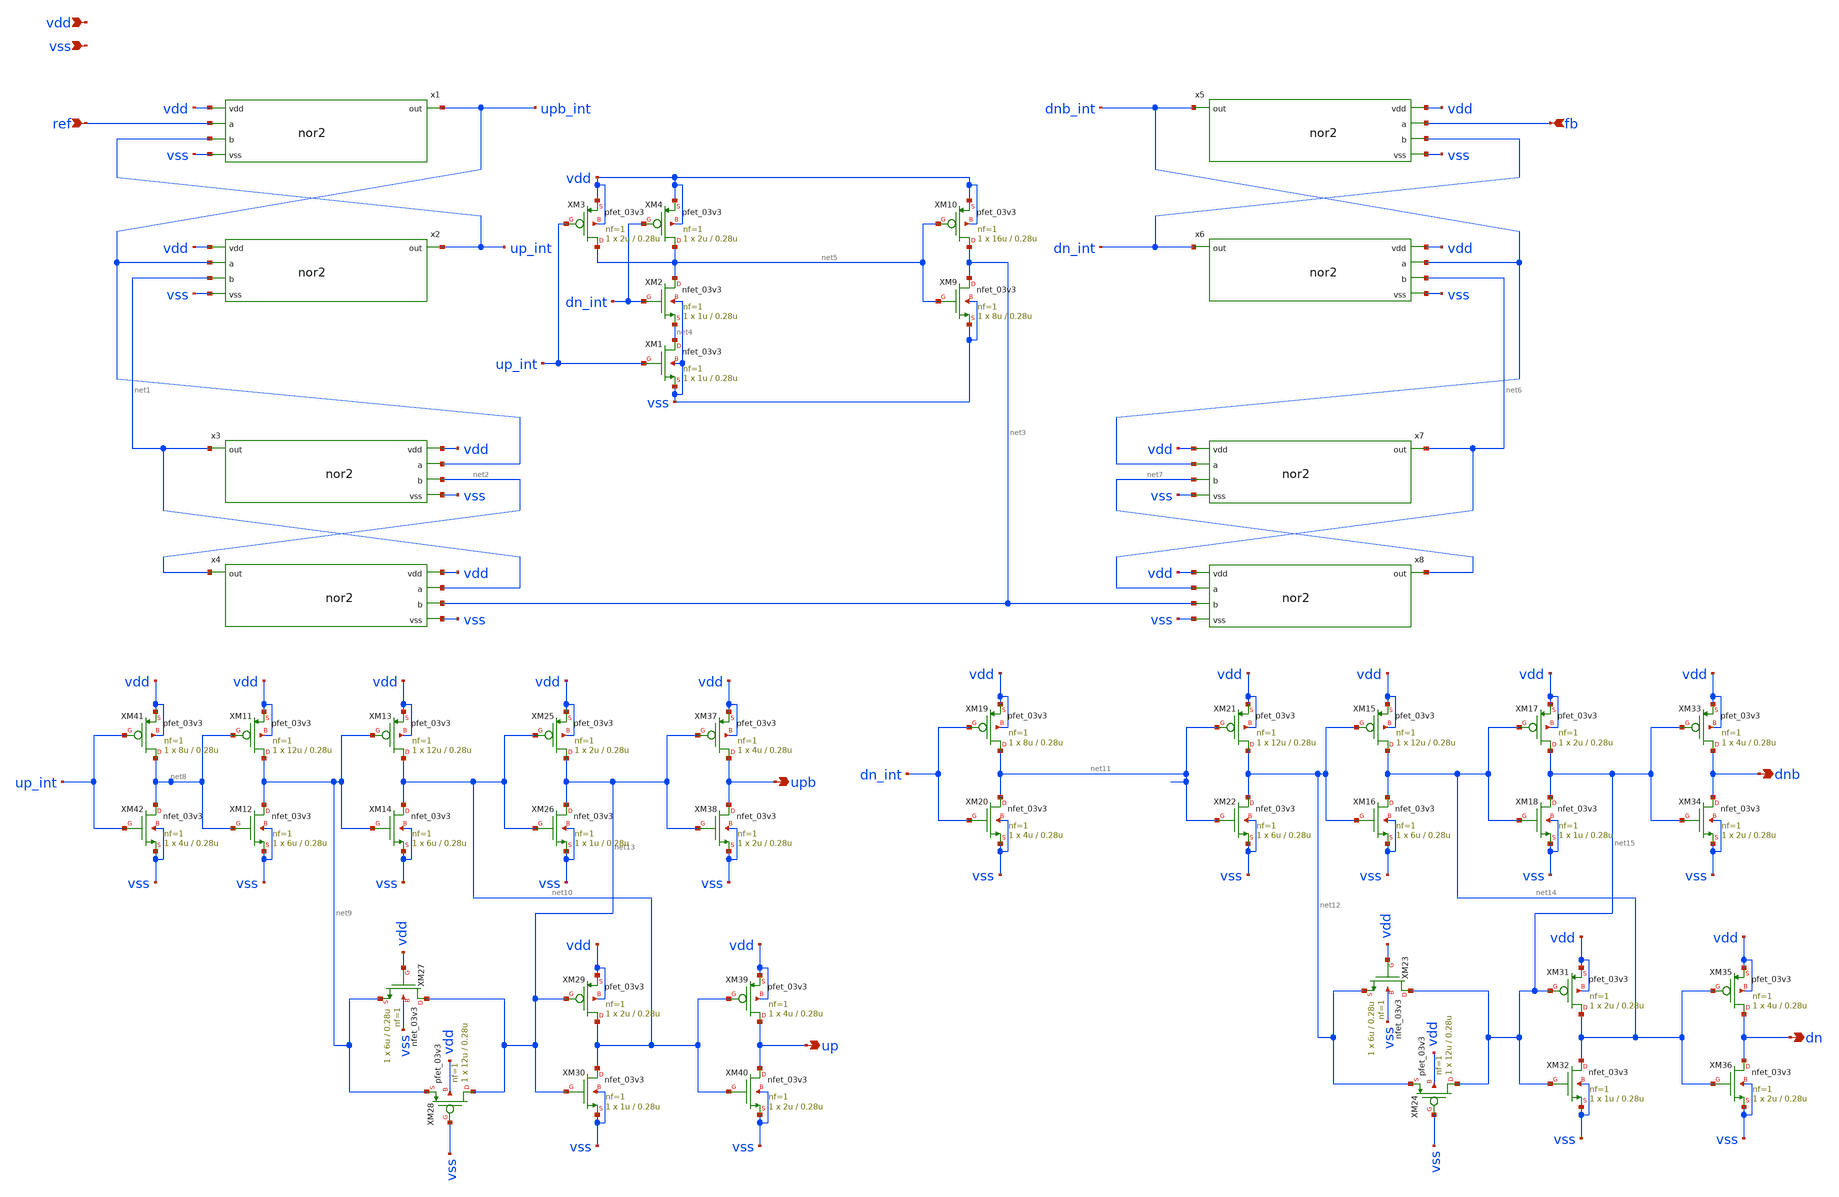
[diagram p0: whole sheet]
** sch_path: xschem/pfd_cmos.sch
**.subckt pfd_cmos ref fb vdd vss up upb dn dnb
*.ipin ref
*.ipin fb
*.ipin vdd
*.ipin vss
*.opin up
*.opin upb
*.opin dn
*.opin dnb
x1 vdd upb_int ref up_int vss nor2
x2 vdd up_int upb_int net1 vss nor2
x3 vdd net1 upb_int net2 vss nor2
x4 vdd net2 net1 net3 vss nor2
XM1 net4 up_int vss vss nfet_03v3 L=0.28u W=1u nf=1 ad='int((nf+1)/2) * W/nf * 0.18u' as='int((nf+2)/2) * W/nf * 0.18u'
+ pd='2*int((nf+1)/2) * (W/nf + 0.18u)' ps='2*int((nf+2)/2) * (W/nf + 0.18u)' nrd='0.18u / W' nrs='0.18u / W'
+ sa=0 sb=0 sd=0 m=1
XM2 net5 dn_int net4 vss nfet_03v3 L=0.28u W=1u nf=1 ad='int((nf+1)/2) * W/nf * 0.18u' as='int((nf+2)/2) * W/nf * 0.18u'
+ pd='2*int((nf+1)/2) * (W/nf + 0.18u)' ps='2*int((nf+2)/2) * (W/nf + 0.18u)' nrd='0.18u / W' nrs='0.18u / W'
+ sa=0 sb=0 sd=0 m=1
XM4 net5 dn_int vdd vdd pfet_03v3 L=0.28u W=2u nf=1 ad='int((nf+1)/2) * W/nf * 0.18u' as='int((nf+2)/2) * W/nf * 0.18u'
+ pd='2*int((nf+1)/2) * (W/nf + 0.18u)' ps='2*int((nf+2)/2) * (W/nf + 0.18u)' nrd='0.18u / W' nrs='0.18u / W'
+ sa=0 sb=0 sd=0 m=1
XM3 net5 up_int vdd vdd pfet_03v3 L=0.28u W=2u nf=1 ad='int((nf+1)/2) * W/nf * 0.18u' as='int((nf+2)/2) * W/nf * 0.18u'
+ pd='2*int((nf+1)/2) * (W/nf + 0.18u)' ps='2*int((nf+2)/2) * (W/nf + 0.18u)' nrd='0.18u / W' nrs='0.18u / W'
+ sa=0 sb=0 sd=0 m=1
x5 vdd dnb_int fb dn_int vss nor2
x6 vdd dn_int dnb_int net6 vss nor2
x7 vdd net6 dnb_int net7 vss nor2
x8 vdd net7 net6 net3 vss nor2
XM9 net3 net5 vss vss nfet_03v3 L=0.28u W=8u nf=1 ad='int((nf+1)/2) * W/nf * 0.18u' as='int((nf+2)/2) * W/nf * 0.18u'
+ pd='2*int((nf+1)/2) * (W/nf + 0.18u)' ps='2*int((nf+2)/2) * (W/nf + 0.18u)' nrd='0.18u / W' nrs='0.18u / W'
+ sa=0 sb=0 sd=0 m=1
XM10 net3 net5 vdd vdd pfet_03v3 L=0.28u W=16u nf=1 ad='int((nf+1)/2) * W/nf * 0.18u' as='int((nf+2)/2) * W/nf * 0.18u'
+ pd='2*int((nf+1)/2) * (W/nf + 0.18u)' ps='2*int((nf+2)/2) * (W/nf + 0.18u)' nrd='0.18u / W' nrs='0.18u / W'
+ sa=0 sb=0 sd=0 m=1
XM11 net9 net8 vdd vdd pfet_03v3 L=0.28u W=12u nf=1 ad='int((nf+1)/2) * W/nf * 0.18u' as='int((nf+2)/2) * W/nf * 0.18u'
+ pd='2*int((nf+1)/2) * (W/nf + 0.18u)' ps='2*int((nf+2)/2) * (W/nf + 0.18u)' nrd='0.18u / W' nrs='0.18u / W'
+ sa=0 sb=0 sd=0 m=1
XM12 net9 net8 vss vss nfet_03v3 L=0.28u W=6u nf=1 ad='int((nf+1)/2) * W/nf * 0.18u' as='int((nf+2)/2) * W/nf * 0.18u'
+ pd='2*int((nf+1)/2) * (W/nf + 0.18u)' ps='2*int((nf+2)/2) * (W/nf + 0.18u)' nrd='0.18u / W' nrs='0.18u / W'
+ sa=0 sb=0 sd=0 m=1
XM13 net10 net9 vdd vdd pfet_03v3 L=0.28u W=12u nf=1 ad='int((nf+1)/2) * W/nf * 0.18u' as='int((nf+2)/2) * W/nf * 0.18u'
+ pd='2*int((nf+1)/2) * (W/nf + 0.18u)' ps='2*int((nf+2)/2) * (W/nf + 0.18u)' nrd='0.18u / W' nrs='0.18u / W'
+ sa=0 sb=0 sd=0 m=1
XM14 net10 net9 vss vss nfet_03v3 L=0.28u W=6u nf=1 ad='int((nf+1)/2) * W/nf * 0.18u' as='int((nf+2)/2) * W/nf * 0.18u'
+ pd='2*int((nf+1)/2) * (W/nf + 0.18u)' ps='2*int((nf+2)/2) * (W/nf + 0.18u)' nrd='0.18u / W' nrs='0.18u / W'
+ sa=0 sb=0 sd=0 m=1
XM19 net11 dn_int vdd vdd pfet_03v3 L=0.28u W=8u nf=1 ad='int((nf+1)/2) * W/nf * 0.18u' as='int((nf+2)/2) * W/nf * 0.18u'
+ pd='2*int((nf+1)/2) * (W/nf + 0.18u)' ps='2*int((nf+2)/2) * (W/nf + 0.18u)' nrd='0.18u / W' nrs='0.18u / W'
+ sa=0 sb=0 sd=0 m=1
XM20 net11 dn_int vss vss nfet_03v3 L=0.28u W=4u nf=1 ad='int((nf+1)/2) * W/nf * 0.18u' as='int((nf+2)/2) * W/nf * 0.18u'
+ pd='2*int((nf+1)/2) * (W/nf + 0.18u)' ps='2*int((nf+2)/2) * (W/nf + 0.18u)' nrd='0.18u / W' nrs='0.18u / W'
+ sa=0 sb=0 sd=0 m=1
XM21 net12 net11 vdd vdd pfet_03v3 L=0.28u W=12u nf=1 ad='int((nf+1)/2) * W/nf * 0.18u' as='int((nf+2)/2) * W/nf * 0.18u'
+ pd='2*int((nf+1)/2) * (W/nf + 0.18u)' ps='2*int((nf+2)/2) * (W/nf + 0.18u)' nrd='0.18u / W' nrs='0.18u / W'
+ sa=0 sb=0 sd=0 m=1
XM22 net12 net11 vss vss nfet_03v3 L=0.28u W=6u nf=1 ad='int((nf+1)/2) * W/nf * 0.18u' as='int((nf+2)/2) * W/nf * 0.18u'
+ pd='2*int((nf+1)/2) * (W/nf + 0.18u)' ps='2*int((nf+2)/2) * (W/nf + 0.18u)' nrd='0.18u / W' nrs='0.18u / W'
+ sa=0 sb=0 sd=0 m=1
XM25 net13 net10 vdd vdd pfet_03v3 L=0.28u W=2u nf=1 ad='int((nf+1)/2) * W/nf * 0.18u' as='int((nf+2)/2) * W/nf * 0.18u'
+ pd='2*int((nf+1)/2) * (W/nf + 0.18u)' ps='2*int((nf+2)/2) * (W/nf + 0.18u)' nrd='0.18u / W' nrs='0.18u / W'
+ sa=0 sb=0 sd=0 m=1
XM26 net13 net10 vss vss nfet_03v3 L=0.28u W=1u nf=1 ad='int((nf+1)/2) * W/nf * 0.18u' as='int((nf+2)/2) * W/nf * 0.18u'
+ pd='2*int((nf+1)/2) * (W/nf + 0.18u)' ps='2*int((nf+2)/2) * (W/nf + 0.18u)' nrd='0.18u / W' nrs='0.18u / W'
+ sa=0 sb=0 sd=0 m=1
XM27 net13 vdd net9 vss nfet_03v3 L=0.28u W=6u nf=1 ad='int((nf+1)/2) * W/nf * 0.18u' as='int((nf+2)/2) * W/nf * 0.18u'
+ pd='2*int((nf+1)/2) * (W/nf + 0.18u)' ps='2*int((nf+2)/2) * (W/nf + 0.18u)' nrd='0.18u / W' nrs='0.18u / W'
+ sa=0 sb=0 sd=0 m=1
XM28 net13 vss net9 vdd pfet_03v3 L=0.28u W=12u nf=1 ad='int((nf+1)/2) * W/nf * 0.18u' as='int((nf+2)/2) * W/nf * 0.18u'
+ pd='2*int((nf+1)/2) * (W/nf + 0.18u)' ps='2*int((nf+2)/2) * (W/nf + 0.18u)' nrd='0.18u / W' nrs='0.18u / W'
+ sa=0 sb=0 sd=0 m=1
XM29 net10 net13 vdd vdd pfet_03v3 L=0.28u W=2u nf=1 ad='int((nf+1)/2) * W/nf * 0.18u' as='int((nf+2)/2) * W/nf * 0.18u'
+ pd='2*int((nf+1)/2) * (W/nf + 0.18u)' ps='2*int((nf+2)/2) * (W/nf + 0.18u)' nrd='0.18u / W' nrs='0.18u / W'
+ sa=0 sb=0 sd=0 m=1
XM30 net10 net13 vss vss nfet_03v3 L=0.28u W=1u nf=1 ad='int((nf+1)/2) * W/nf * 0.18u' as='int((nf+2)/2) * W/nf * 0.18u'
+ pd='2*int((nf+1)/2) * (W/nf + 0.18u)' ps='2*int((nf+2)/2) * (W/nf + 0.18u)' nrd='0.18u / W' nrs='0.18u / W'
+ sa=0 sb=0 sd=0 m=1
XM15 net14 net12 vdd vdd pfet_03v3 L=0.28u W=12u nf=1 ad='int((nf+1)/2) * W/nf * 0.18u' as='int((nf+2)/2) * W/nf * 0.18u'
+ pd='2*int((nf+1)/2) * (W/nf + 0.18u)' ps='2*int((nf+2)/2) * (W/nf + 0.18u)' nrd='0.18u / W' nrs='0.18u / W'
+ sa=0 sb=0 sd=0 m=1
XM16 net14 net12 vss vss nfet_03v3 L=0.28u W=6u nf=1 ad='int((nf+1)/2) * W/nf * 0.18u' as='int((nf+2)/2) * W/nf * 0.18u'
+ pd='2*int((nf+1)/2) * (W/nf + 0.18u)' ps='2*int((nf+2)/2) * (W/nf + 0.18u)' nrd='0.18u / W' nrs='0.18u / W'
+ sa=0 sb=0 sd=0 m=1
XM17 net15 net14 vdd vdd pfet_03v3 L=0.28u W=2u nf=1 ad='int((nf+1)/2) * W/nf * 0.18u' as='int((nf+2)/2) * W/nf * 0.18u'
+ pd='2*int((nf+1)/2) * (W/nf + 0.18u)' ps='2*int((nf+2)/2) * (W/nf + 0.18u)' nrd='0.18u / W' nrs='0.18u / W'
+ sa=0 sb=0 sd=0 m=1
XM18 net15 net14 vss vss nfet_03v3 L=0.28u W=1u nf=1 ad='int((nf+1)/2) * W/nf * 0.18u' as='int((nf+2)/2) * W/nf * 0.18u'
+ pd='2*int((nf+1)/2) * (W/nf + 0.18u)' ps='2*int((nf+2)/2) * (W/nf + 0.18u)' nrd='0.18u / W' nrs='0.18u / W'
+ sa=0 sb=0 sd=0 m=1
XM23 net15 vdd net12 vss nfet_03v3 L=0.28u W=6u nf=1 ad='int((nf+1)/2) * W/nf * 0.18u' as='int((nf+2)/2) * W/nf * 0.18u'
+ pd='2*int((nf+1)/2) * (W/nf + 0.18u)' ps='2*int((nf+2)/2) * (W/nf + 0.18u)' nrd='0.18u / W' nrs='0.18u / W'
+ sa=0 sb=0 sd=0 m=1
XM24 net15 vss net12 vdd pfet_03v3 L=0.28u W=12u nf=1 ad='int((nf+1)/2) * W/nf * 0.18u' as='int((nf+2)/2) * W/nf * 0.18u'
+ pd='2*int((nf+1)/2) * (W/nf + 0.18u)' ps='2*int((nf+2)/2) * (W/nf + 0.18u)' nrd='0.18u / W' nrs='0.18u / W'
+ sa=0 sb=0 sd=0 m=1
XM31 net14 net15 vdd vdd pfet_03v3 L=0.28u W=2u nf=1 ad='int((nf+1)/2) * W/nf * 0.18u' as='int((nf+2)/2) * W/nf * 0.18u'
+ pd='2*int((nf+1)/2) * (W/nf + 0.18u)' ps='2*int((nf+2)/2) * (W/nf + 0.18u)' nrd='0.18u / W' nrs='0.18u / W'
+ sa=0 sb=0 sd=0 m=1
XM32 net14 net15 vss vss nfet_03v3 L=0.28u W=1u nf=1 ad='int((nf+1)/2) * W/nf * 0.18u' as='int((nf+2)/2) * W/nf * 0.18u'
+ pd='2*int((nf+1)/2) * (W/nf + 0.18u)' ps='2*int((nf+2)/2) * (W/nf + 0.18u)' nrd='0.18u / W' nrs='0.18u / W'
+ sa=0 sb=0 sd=0 m=1
XM33 dnb net15 vdd vdd pfet_03v3 L=0.28u W=4u nf=1 ad='int((nf+1)/2) * W/nf * 0.18u' as='int((nf+2)/2) * W/nf * 0.18u'
+ pd='2*int((nf+1)/2) * (W/nf + 0.18u)' ps='2*int((nf+2)/2) * (W/nf + 0.18u)' nrd='0.18u / W' nrs='0.18u / W'
+ sa=0 sb=0 sd=0 m=1
XM34 dnb net15 vss vss nfet_03v3 L=0.28u W=2u nf=1 ad='int((nf+1)/2) * W/nf * 0.18u' as='int((nf+2)/2) * W/nf * 0.18u'
+ pd='2*int((nf+1)/2) * (W/nf + 0.18u)' ps='2*int((nf+2)/2) * (W/nf + 0.18u)' nrd='0.18u / W' nrs='0.18u / W'
+ sa=0 sb=0 sd=0 m=1
XM35 dn net14 vdd vdd pfet_03v3 L=0.28u W=4u nf=1 ad='int((nf+1)/2) * W/nf * 0.18u' as='int((nf+2)/2) * W/nf * 0.18u'
+ pd='2*int((nf+1)/2) * (W/nf + 0.18u)' ps='2*int((nf+2)/2) * (W/nf + 0.18u)' nrd='0.18u / W' nrs='0.18u / W'
+ sa=0 sb=0 sd=0 m=1
XM36 dn net14 vss vss nfet_03v3 L=0.28u W=2u nf=1 ad='int((nf+1)/2) * W/nf * 0.18u' as='int((nf+2)/2) * W/nf * 0.18u'
+ pd='2*int((nf+1)/2) * (W/nf + 0.18u)' ps='2*int((nf+2)/2) * (W/nf + 0.18u)' nrd='0.18u / W' nrs='0.18u / W'
+ sa=0 sb=0 sd=0 m=1
XM37 upb net13 vdd vdd pfet_03v3 L=0.28u W=4u nf=1 ad='int((nf+1)/2) * W/nf * 0.18u' as='int((nf+2)/2) * W/nf * 0.18u'
+ pd='2*int((nf+1)/2) * (W/nf + 0.18u)' ps='2*int((nf+2)/2) * (W/nf + 0.18u)' nrd='0.18u / W' nrs='0.18u / W'
+ sa=0 sb=0 sd=0 m=1
XM38 upb net13 vss vss nfet_03v3 L=0.28u W=2u nf=1 ad='int((nf+1)/2) * W/nf * 0.18u' as='int((nf+2)/2) * W/nf * 0.18u'
+ pd='2*int((nf+1)/2) * (W/nf + 0.18u)' ps='2*int((nf+2)/2) * (W/nf + 0.18u)' nrd='0.18u / W' nrs='0.18u / W'
+ sa=0 sb=0 sd=0 m=1
XM39 up net10 vdd vdd pfet_03v3 L=0.28u W=4u nf=1 ad='int((nf+1)/2) * W/nf * 0.18u' as='int((nf+2)/2) * W/nf * 0.18u'
+ pd='2*int((nf+1)/2) * (W/nf + 0.18u)' ps='2*int((nf+2)/2) * (W/nf + 0.18u)' nrd='0.18u / W' nrs='0.18u / W'
+ sa=0 sb=0 sd=0 m=1
XM40 up net10 vss vss nfet_03v3 L=0.28u W=2u nf=1 ad='int((nf+1)/2) * W/nf * 0.18u' as='int((nf+2)/2) * W/nf * 0.18u'
+ pd='2*int((nf+1)/2) * (W/nf + 0.18u)' ps='2*int((nf+2)/2) * (W/nf + 0.18u)' nrd='0.18u / W' nrs='0.18u / W'
+ sa=0 sb=0 sd=0 m=1
XM41 net8 up_int vdd vdd pfet_03v3 L=0.28u W=8u nf=1 ad='int((nf+1)/2) * W/nf * 0.18u' as='int((nf+2)/2) * W/nf * 0.18u'
+ pd='2*int((nf+1)/2) * (W/nf + 0.18u)' ps='2*int((nf+2)/2) * (W/nf + 0.18u)' nrd='0.18u / W' nrs='0.18u / W'
+ sa=0 sb=0 sd=0 m=1
XM42 net8 up_int vss vss nfet_03v3 L=0.28u W=4u nf=1 ad='int((nf+1)/2) * W/nf * 0.18u' as='int((nf+2)/2) * W/nf * 0.18u'
+ pd='2*int((nf+1)/2) * (W/nf + 0.18u)' ps='2*int((nf+2)/2) * (W/nf + 0.18u)' nrd='0.18u / W' nrs='0.18u / W'
+ sa=0 sb=0 sd=0 m=1
**.ends

* expanding   symbol:  nor2.sym # of pins=5
** sym_path: xschem/nor2.sym
** sch_path: xschem/nor2.sch
.subckt nor2 vdd out a b vss
*.ipin a
*.ipin b
*.ipin vss
*.ipin vdd
*.opin out
XM1 out b vss vss nfet_03v3 L=0.28u W=1u nf=1 ad='int((nf+1)/2) * W/nf * 0.18u' as='int((nf+2)/2) * W/nf * 0.18u'
+ pd='2*int((nf+1)/2) * (W/nf + 0.18u)' ps='2*int((nf+2)/2) * (W/nf + 0.18u)' nrd='0.18u / W' nrs='0.18u / W'
+ sa=0 sb=0 sd=0 m=1
XM2 out a vss vss nfet_03v3 L=0.28u W=1u nf=1 ad='int((nf+1)/2) * W/nf * 0.18u' as='int((nf+2)/2) * W/nf * 0.18u'
+ pd='2*int((nf+1)/2) * (W/nf + 0.18u)' ps='2*int((nf+2)/2) * (W/nf + 0.18u)' nrd='0.18u / W' nrs='0.18u / W'
+ sa=0 sb=0 sd=0 m=1
XM3 out a net1 vdd pfet_03v3 L=0.28u W=2u nf=1 ad='int((nf+1)/2) * W/nf * 0.18u' as='int((nf+2)/2) * W/nf * 0.18u'
+ pd='2*int((nf+1)/2) * (W/nf + 0.18u)' ps='2*int((nf+2)/2) * (W/nf + 0.18u)' nrd='0.18u / W' nrs='0.18u / W'
+ sa=0 sb=0 sd=0 m=1
XM4 net1 b vdd vdd pfet_03v3 L=0.28u W=2u nf=1 ad='int((nf+1)/2) * W/nf * 0.18u' as='int((nf+2)/2) * W/nf * 0.18u'
+ pd='2*int((nf+1)/2) * (W/nf + 0.18u)' ps='2*int((nf+2)/2) * (W/nf + 0.18u)' nrd='0.18u / W' nrs='0.18u / W'
+ sa=0 sb=0 sd=0 m=1
.ends

.end
